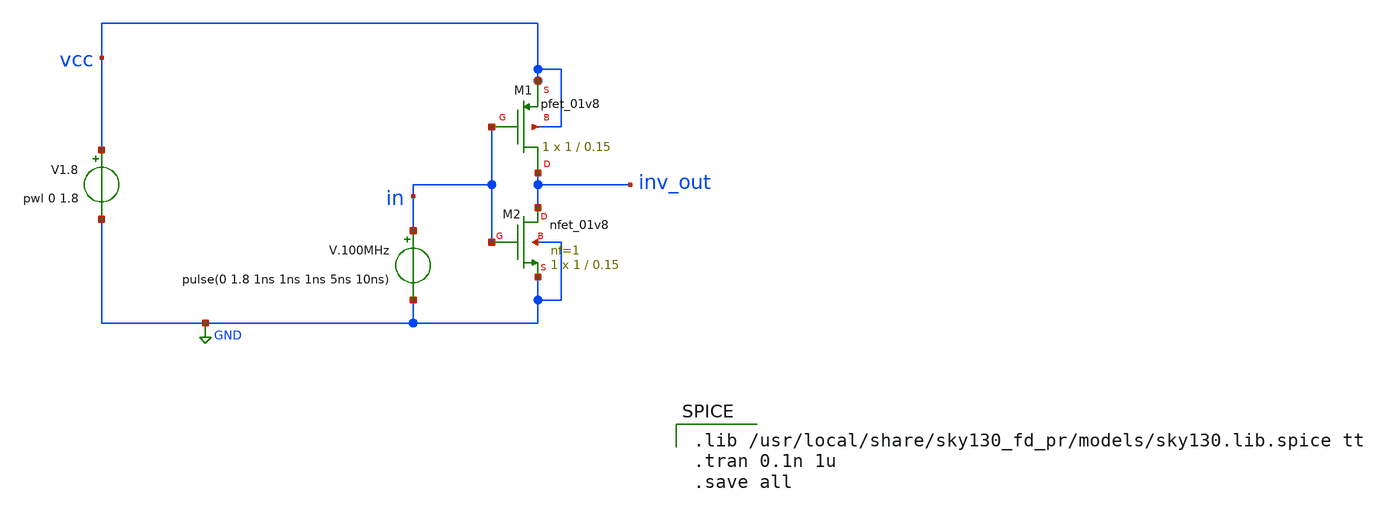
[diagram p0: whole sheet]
** sch_path: schematic/xschem/basic-inverter.sch
**.subckt basic-inverter
V.100MHz in GND pulse(0 1.8 1ns 1ns 1ns 5ns 10ns)
V1.8 vcc GND pwl 0 1.8
XM2 inv_out in GND GND sky130_fd_pr__nfet_01v8 L=0.15 W=1 nf=1 ad='W * 0.29' as='W * 0.29' pd='W + 2 * 0.29'
+ ps='W + 2 * 0.29' nrd=0 nrs=0 sa=0 sb=0 sd=0 mult=1 m=1
XM1 inv_out in vcc vcc sky130_fd_pr__pfet_01v8 W=1 L=0.15 ad='W * 0.29' pd='W + 2 * 0.29' as='W * 0.29'
+ ps='W + 2 * 0.29' nrd=0 nrs=0 sa=0 sb=0 sd=0 nf=1 mult=1
**** begin user architecture code

.lib /usr/local/share/sky130_fd_pr/models/sky130.lib.spice tt
.tran 0.1n 1u
.save all

**** end user architecture code
**.ends
.GLOBAL GND
.end
